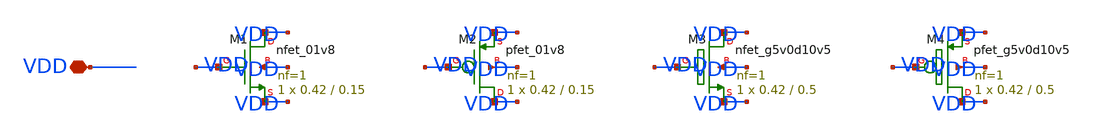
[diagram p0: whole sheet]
** sch_path: sky130A/schematic/xschem/sky130_short1.sch
**.subckt sky130_short1 VDD
*.iopin VDD
XM1 VDD VDD VDD VDD sky130_fd_pr__nfet_01v8 L=0.15 W=0.42 nf=1 ad='int((1 + 1)/2) * 0.42 / 1 * 0.29'
+ as='int((1 + 2)/2) * 0.42 / 1 * 0.29' pd='2*int((1 + 1)/2) * (0.42 / 1 + 0.29)' ps='2*int((1 + 2)/2) * (0.42 / 1 + 0.29)'
+ nrd='0.29 / 0.42 ' nrs='0.29 / 0.42 ' sa=0 sb=0 sd=0 mult=1 m=1
XM2 VDD VDD VDD VDD sky130_fd_pr__pfet_01v8 L=0.15 W=0.42 nf=1 ad='int((1 + 1)/2) * 0.42 / 1 * 0.29'
+ as='int((1 + 2)/2) * 0.42 / 1 * 0.29' pd='2*int((1 + 1)/2) * (0.42 / 1 + 0.29)' ps='2*int((1 + 2)/2) * (0.42 / 1 + 0.29)'
+ nrd='0.29 / 0.42 ' nrs='0.29 / 0.42 ' sa=0 sb=0 sd=0 mult=1 m=1
XM3 VDD VDD VDD VDD sky130_fd_pr__nfet_g5v0d10v5 L=0.5 W=0.42 nf=1 ad='int((1 + 1)/2) * 0.42 / 1 * 0.29'
+ as='int((1 + 2)/2) * 0.42 / 1 * 0.29' pd='2*int((1 + 1)/2) * (0.42 / 1 + 0.29)' ps='2*int((1 + 2)/2) * (0.42 / 1 + 0.29)'
+ nrd='0.29 / 0.42 ' nrs='0.29 / 0.42 ' sa=0 sb=0 sd=0 mult=1 m=1
XM4 VDD VDD VDD VDD sky130_fd_pr__pfet_g5v0d10v5 L=0.5 W=0.42 nf=1 ad='int((1 + 1)/2) * 0.42 / 1 * 0.29'
+ as='int((1 + 2)/2) * 0.42 / 1 * 0.29' pd='2*int((1 + 1)/2) * (0.42 / 1 + 0.29)' ps='2*int((1 + 2)/2) * (0.42 / 1 + 0.29)'
+ nrd='0.29 / 0.42 ' nrs='0.29 / 0.42 ' sa=0 sb=0 sd=0 mult=1 m=1
**.ends
.end
